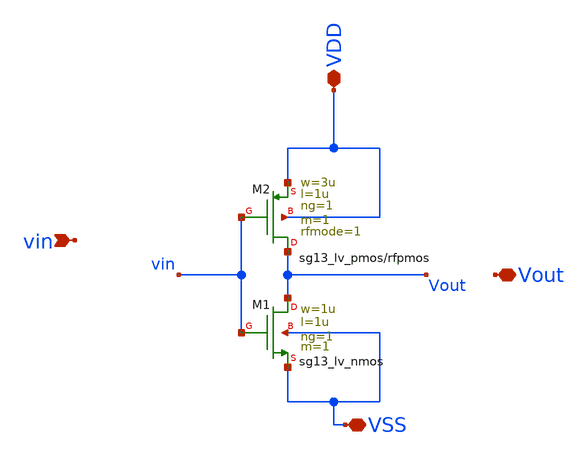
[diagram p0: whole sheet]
** sch_path: Lab2/inverter22.sch
**.subckt inverter22 vin Vout VDD VSS
*.ipin vin
*.iopin Vout
*.iopin VDD
*.iopin VSS
XM1 Vout vin VSS VSS sg13_lv_nmos w=1u l=1u ng=1 m=1 mm_ok=1
XM2 Vout vin VDD VDD sg13_lv_pmos w=3u l=1u ng=1 m=1 rfmode=1 mm_ok=1
**.ends
.end
